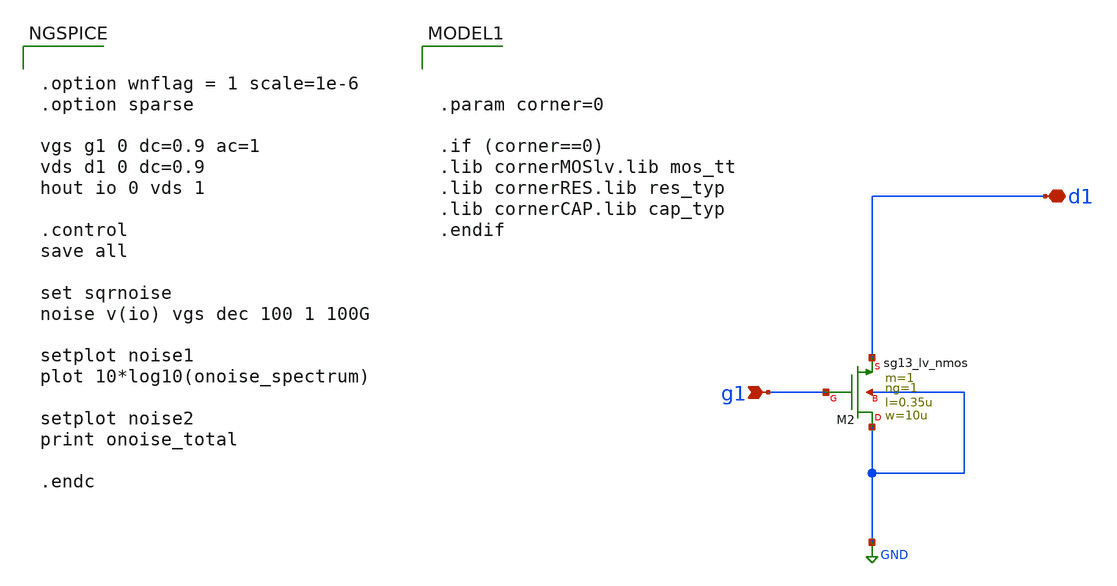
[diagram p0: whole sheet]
** sch_path: xschem/Tareas/Tarea_2/mos-noise-corners_IHP_jm.sch
**.subckt mos-noise-corners_IHP_jm g1 d1
*.ipin g1
*.iopin d1
XM2 GND g1 d1 GND sg13_lv_nmos w=10u l=0.35u ng=1 m=1 mm_ok=1
**** begin user architecture code


.option wnflag = 1 scale=1e-6
.option sparse

vgs g1 0 dc=0.9 ac=1
vds d1 0 dc=0.9
hout io 0 vds 1

.control
save all

set sqrnoise
noise v(io) vgs dec 100 1 100G

setplot noise1
plot 10*log10(onoise_spectrum)

setplot noise2
print onoise_total

.endc




.param corner=0

.if (corner==0)
.lib cornerMOSlv.lib mos_tt
.lib cornerRES.lib res_typ
.lib cornerCAP.lib cap_typ
.endif

**** end user architecture code
**.ends
.GLOBAL GND
.end
